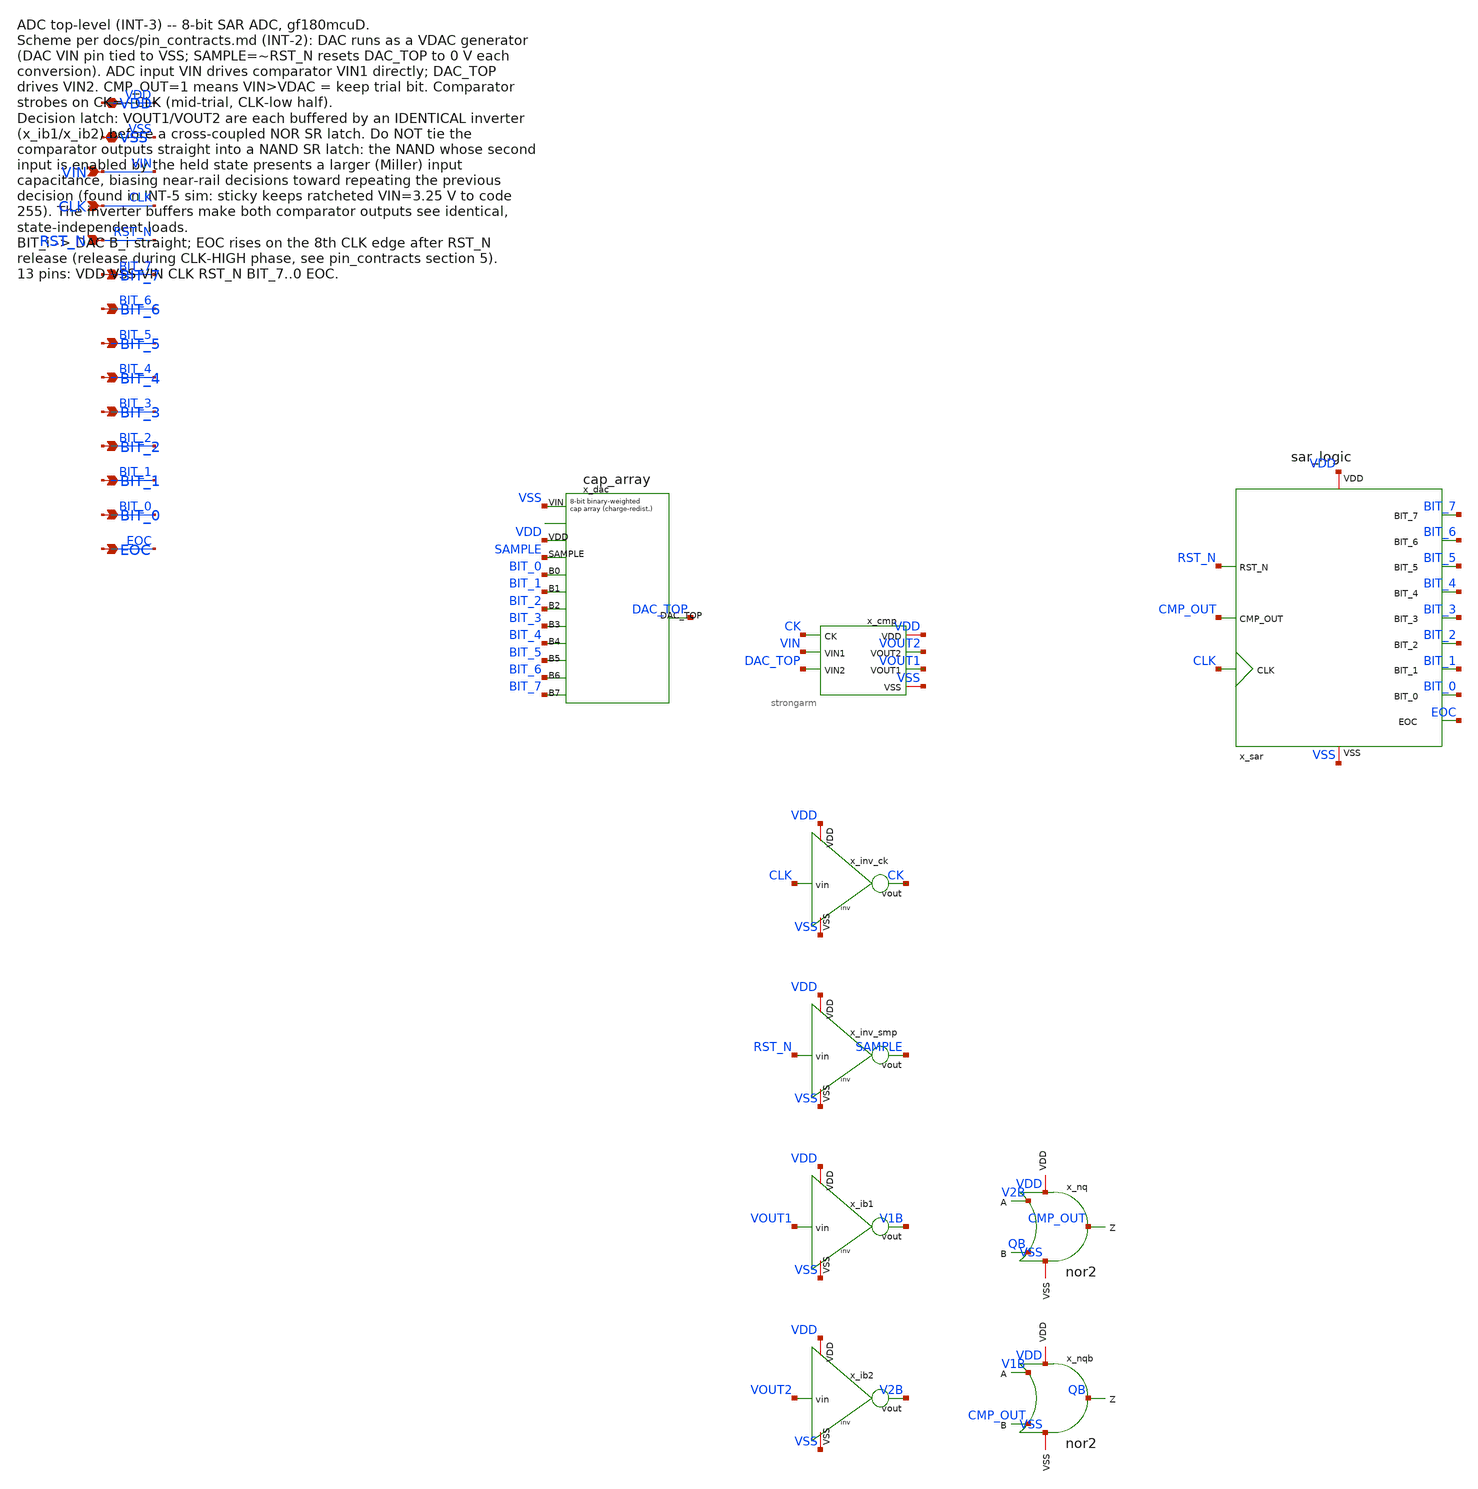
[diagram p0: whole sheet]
** sch_path: adc_top/schematic/adc_top.sch
**.subckt adc_top VDD VSS VIN CLK RST_N BIT_7 BIT_6 BIT_5 BIT_4 BIT_3 BIT_2 BIT_1 BIT_0 EOC
*.iopin VDD
*.iopin VSS
*.ipin VIN
*.ipin CLK
*.ipin RST_N
*.opin BIT_7
*.opin BIT_6
*.opin BIT_5
*.opin BIT_4
*.opin BIT_3
*.opin BIT_2
*.opin BIT_1
*.opin BIT_0
*.opin EOC
x_dac VSS VDD SAMPLE BIT_0 BIT_1 BIT_2 BIT_3 BIT_4 BIT_5 BIT_6 BIT_7 DAC_TOP cap_array
x_cmp VDD CK VOUT2 VOUT1 VIN DAC_TOP VSS strongarm
x_sar VDD VSS BIT_7 BIT_6 BIT_5 BIT_4 BIT_3 BIT_2 BIT_1 BIT_0 EOC RST_N CMP_OUT CLK sar_logic
x_inv_ck VDD CLK CK VSS inv
x_inv_smp VDD RST_N SAMPLE VSS inv
x_ib1 VDD VOUT1 V1B VSS inv
x_ib2 VDD VOUT2 V2B VSS inv
x_nq VDD V2B QB CMP_OUT VSS nor2
x_nqb VDD V1B CMP_OUT QB VSS nor2
**.ends
.end
